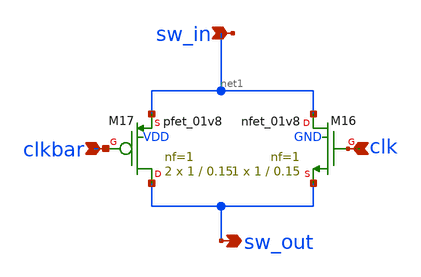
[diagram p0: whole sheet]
** sch_path: closed_loop_symbol_view_simulation/sw_txgate.sch
**.subckt sw_txgate sw_out sw_in clkbar clk
*.opin sw_out
*.ipin sw_in
*.ipin clkbar
*.ipin clk
XM16 net1 net2 sw_out GND sky130_fd_pr__nfet_01v8 L=0.15 W=1 nf=1 ad='int((nf+1)/2) * W/nf * 0.29' as='int((nf+2)/2) * W/nf * 0.29'
+ pd='2*int((nf+1)/2) * (W/nf + 0.29)' ps='2*int((nf+2)/2) * (W/nf + 0.29)' nrd='0.29 / W' nrs='0.29 / W'
+ sa=0 sb=0 sd=0 mult=1 m=1
XM17 sw_out clkbar net1 VDD sky130_fd_pr__pfet_01v8 L=0.15 W=1 nf=1 ad='int((nf+1)/2) * W/nf * 0.29'
+ as='int((nf+2)/2) * W/nf * 0.29' pd='2*int((nf+1)/2) * (W/nf + 0.29)' ps='2*int((nf+2)/2) * (W/nf + 0.29)'
+ nrd='0.29 / W' nrs='0.29 / W' sa=0 sb=0 sd=0 mult=2 m=2
**.ends
.end
